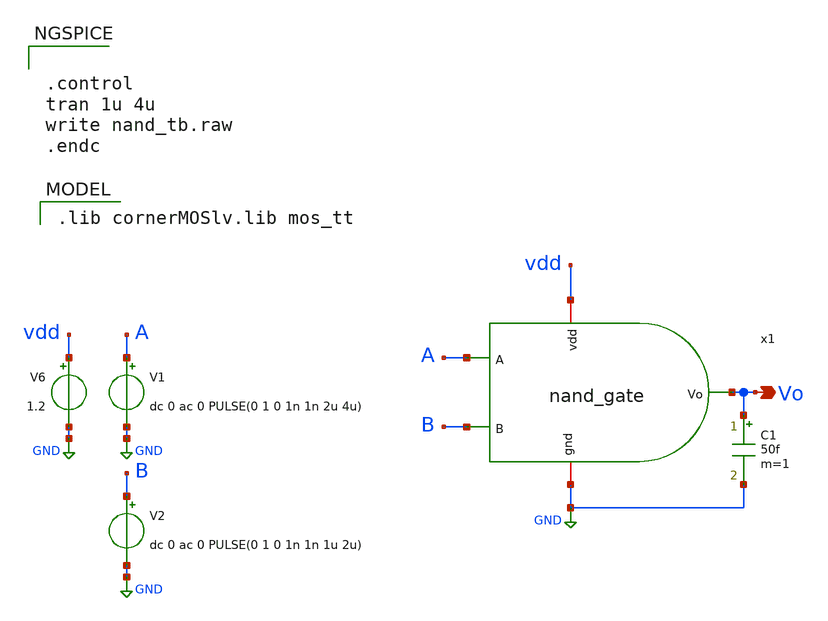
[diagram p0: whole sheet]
** sch_path: modules/module_3_8_bit_SAR_ADC/part_2_digital_comps/nand_gate/testbench/nand_tb.sch
**.subckt nand_tb Vo
*.opin Vo
V1 A GND dc 0 ac 0 PULSE(0 1 0 1n 1n 2u 4u)
V6 vdd GND 1.2
V2 B GND dc 0 ac 0 PULSE(0 1 0 1n 1n 1u 2u)
x1 vdd Vo B A GND nand_gate
C1 Vo GND 50f m=1
**** begin user architecture code


.control
tran 1u 4u
write nand_tb.raw
.endc


 .lib cornerMOSlv.lib mos_tt

**** end user architecture code
**.ends

* expanding   symbol:
*+  /home/pedersen/projects/IHP-AnalogAcademy/modules/module_3_8_bit_SAR_ADC/part_2_digital_comps/nand_gate/schematic/nand_gate.sym # of pins=5
** sym_path: modules/module_3_8_bit_SAR_ADC/part_2_digital_comps/nand_gate/schematic/nand_gate.sym
** sch_path: modules/module_3_8_bit_SAR_ADC/part_2_digital_comps/nand_gate/schematic/nand_gate.sch
.subckt nand_gate vdd Vo B A gnd
*.iopin vdd
*.iopin gnd
*.ipin A
*.opin Vo
*.ipin B
XM5 Vo A vdd vdd sg13_lv_pmos w=0.5u l=0.13u ng=1 m=1 mm_ok=1
XM6 Vo A net1 gnd sg13_lv_nmos w=0.25u l=0.13u ng=1 m=1 mm_ok=1
XM1 net1 B gnd gnd sg13_lv_nmos w=0.25u l=0.13u ng=1 m=1 mm_ok=1
XM2 Vo B vdd vdd sg13_lv_pmos w=0.5u l=0.13u ng=1 m=1 mm_ok=1
.ends

.GLOBAL GND
.end
